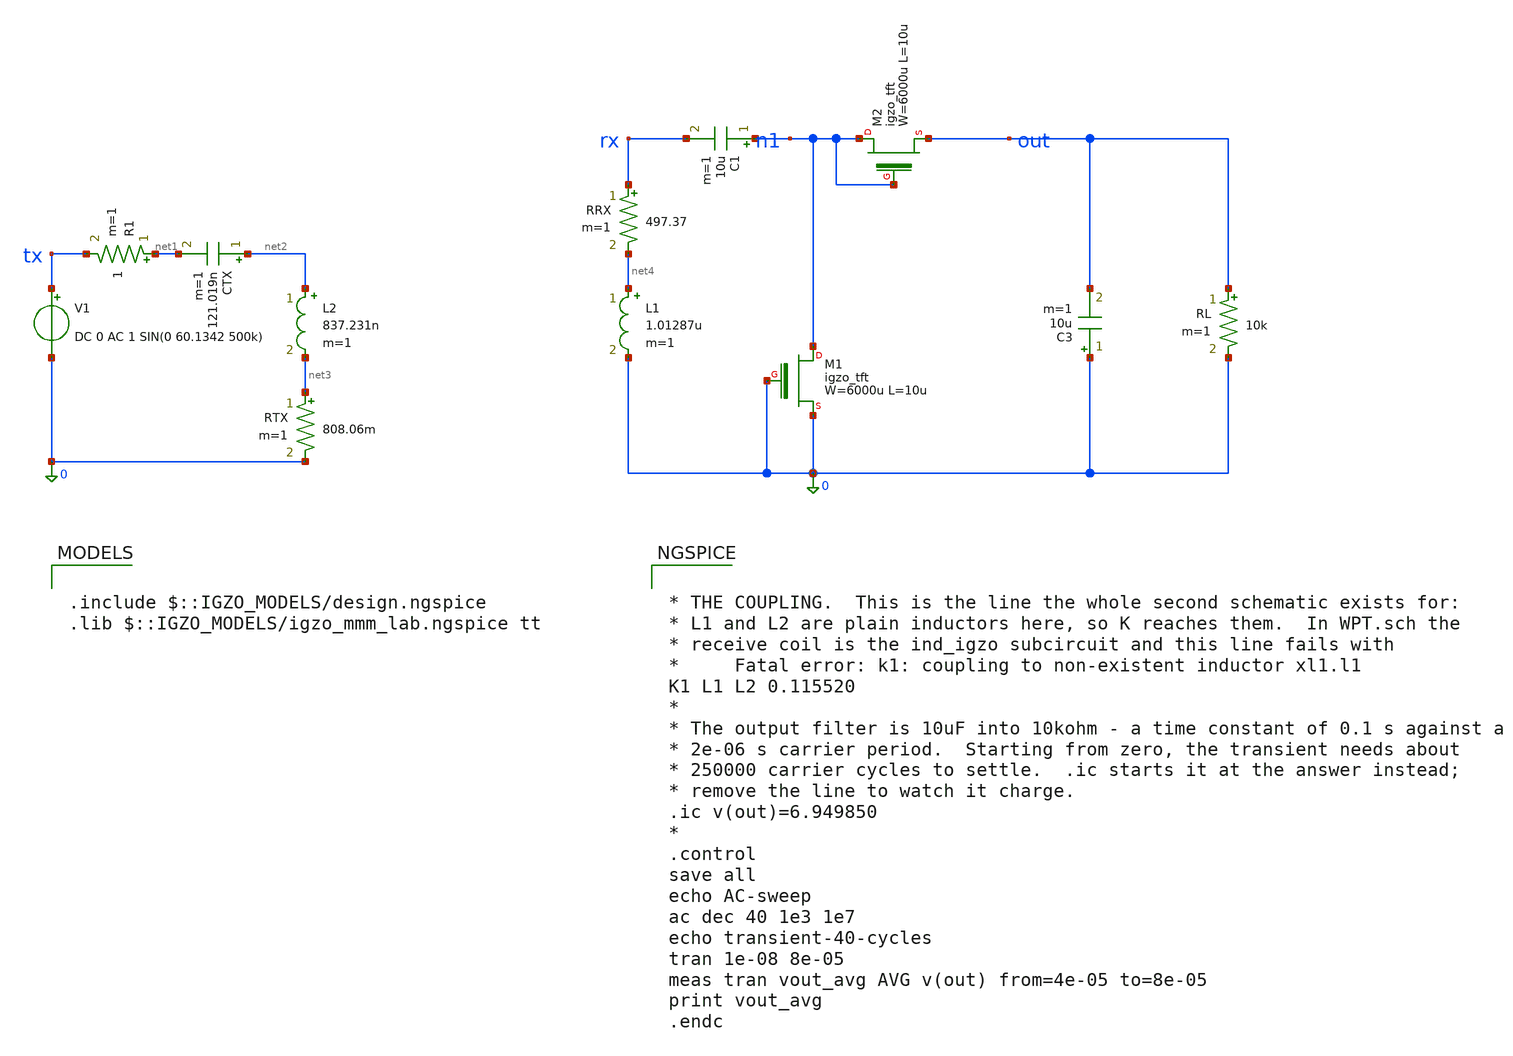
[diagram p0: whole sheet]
** sch_path: WPT/WPT_sim.sch
**.subckt WPT_sim
L1 net4 0 1.01287u m=1
RRX rx net4 497.37 m=1
C1 n1 rx 10u m=1
XM1 n1 0 0 igzo_tft W=6000u L=10u ov=2u nf=1 m=1
XM2 n1 n1 out igzo_tft W=6000u L=10u ov=2u nf=1 m=1
C3 0 out 10u m=1
RL out 0 10k m=1
V1 tx 0 DC 0 AC 1 SIN(0 60.1342 500k)
.save i(v1)
R1 net1 tx 1 m=1
CTX net2 net1 121.019n m=1
L2 net2 net3 837.231n m=1
RTX net3 0 808.06m m=1
**** begin user architecture code

.include $::IGZO_MODELS/design.ngspice
.lib $::IGZO_MODELS/igzo_mmm_lab.ngspice tt



* THE COUPLING.  This is the line the whole second schematic exists for:
* L1 and L2 are plain inductors here, so K reaches them.  In WPT.sch the
* receive coil is the ind_igzo subcircuit and this line fails with
*     Fatal error: k1: coupling to non-existent inductor xl1.l1
K1 L1 L2 0.115520
*
* The output filter is 10uF into 10kohm - a time constant of 0.1 s against a
* 2e-06 s carrier period.  Starting from zero, the transient needs about
* 250000 carrier cycles to settle.  .ic starts it at the answer instead;
* remove the line to watch it charge.
.ic v(out)=6.949850
*
.control
save all
echo AC-sweep
ac dec 40 1e3 1e7
echo transient-40-cycles
tran 1e-08 8e-05
meas tran vout_avg AVG v(out) from=4e-05 to=8e-05
print vout_avg
.endc


**** end user architecture code
**.ends
.end
